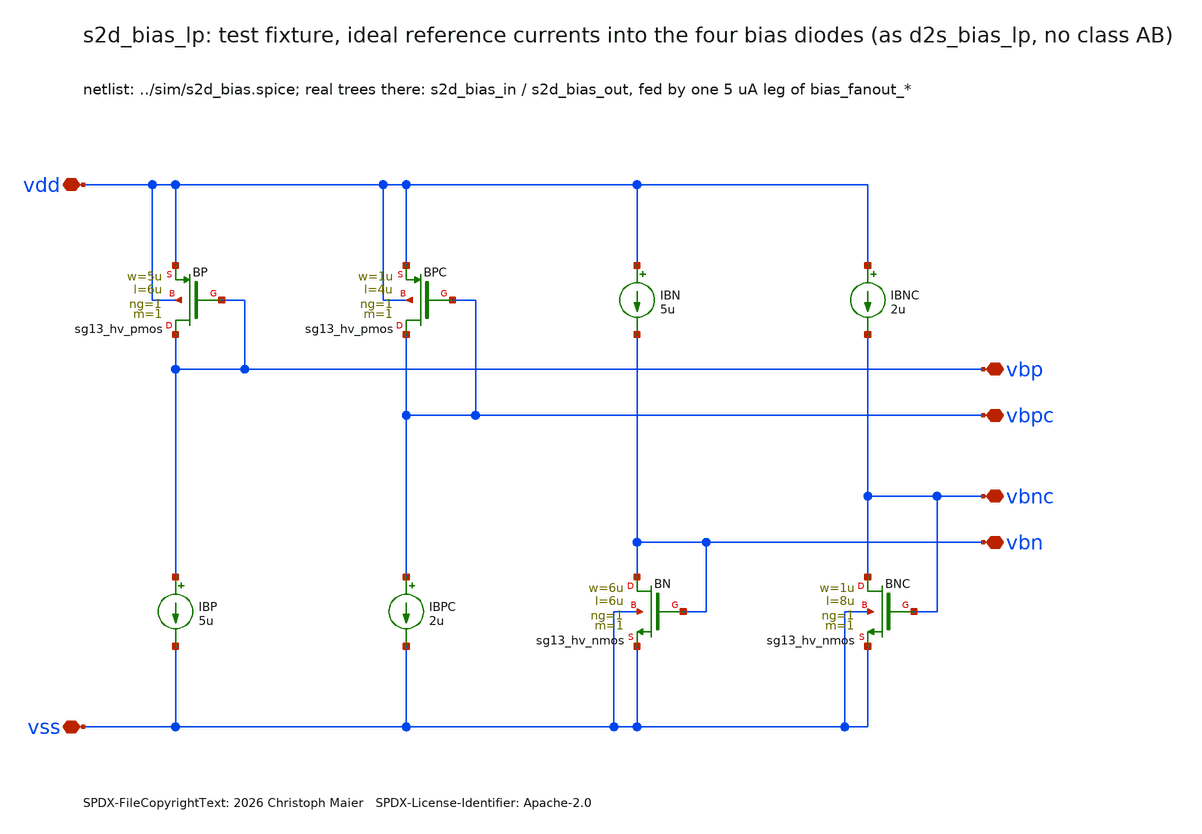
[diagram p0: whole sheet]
** sch_path: sudelbuecher/design_considerations/s2d_input_buffer/xschem/s2d_bias_lp.sch
* SPDX-FileCopyrightText: 2026 Christoph Maier SPDX-License-Identifier: Apache-2.0
**.subckt s2d_bias_lp vdd vss vbp vbn vbpc vbnc
*.iopin vdd
*.iopin vss
*.iopin vbp
*.iopin vbn
*.iopin vbpc
*.iopin vbnc
XBP vbp vbp vdd vdd sg13_hv_pmos w=5u l=6u ng=1 m=1 mm_ok=1
IBP vbp vss 5u
XBPC vbpc vbpc vdd vdd sg13_hv_pmos w=1u l=4u ng=1 m=1 mm_ok=1
IBPC vbpc vss 2u
IBN vdd vbn 5u
XBN vbn vbn vss vss sg13_hv_nmos w=6u l=6u ng=1 m=1 mm_ok=1
IBNC vdd vbnc 2u
XBNC vbnc vbnc vss vss sg13_hv_nmos w=1u l=8u ng=1 m=1 mm_ok=1
**.ends
.end
